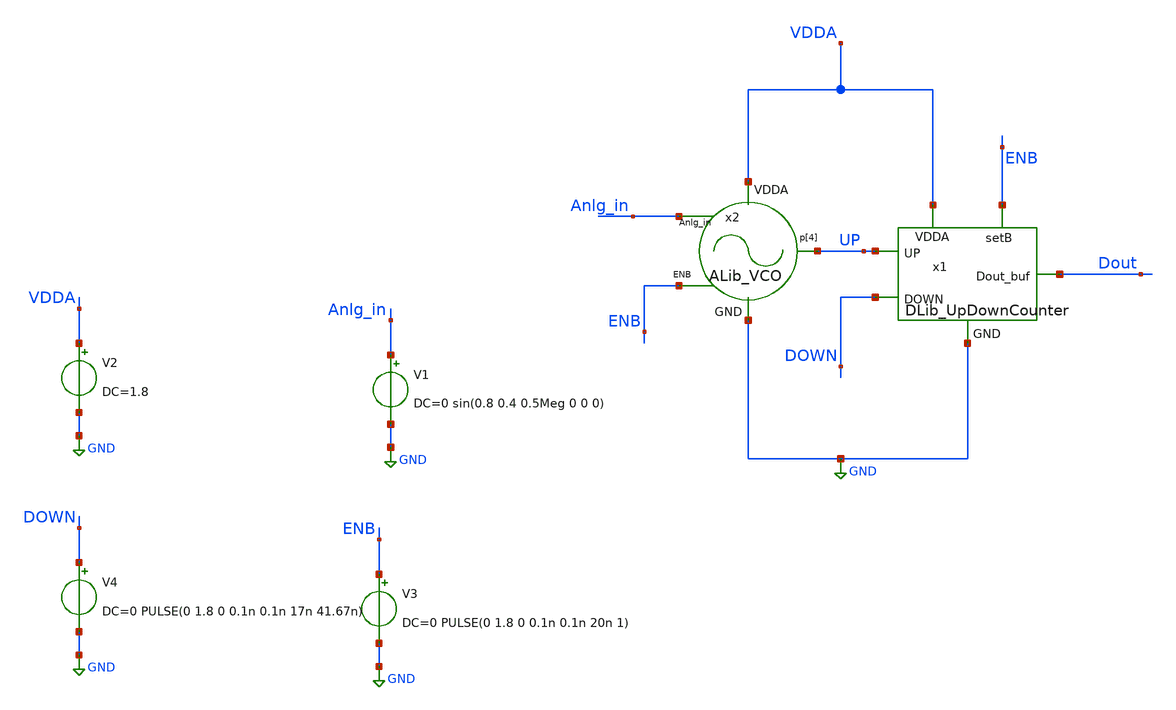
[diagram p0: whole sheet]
** sch_path: xschem/tb/DLib_UpDownCounter_tb.sch
**.subckt DLib_UpDownCounter_tb
x2 Anlg_in ENB UP VDDA GND ALib_VCO
x1 UP DOWN ENB Dout VDDA GND DLib_UpDownCounter
V1 Anlg_in GND DC=0 sin(0.8 0.4 0.5Meg 0 0 0)
V2 VDDA GND DC=1.8
V3 ENB GND DC=0 PULSE(0 1.8 0 0.1n 0.1n 20n 1)
V4 DOWN GND DC=0 PULSE(0 1.8 0 0.1n 0.1n 17n 41.67n)
**** begin user architecture code


.lib /home/dkits/openpdks/sky130A/libs.tech/ngspice/sky130.lib.spice tt
.inc /home/dkits/openpdks/sky130A/libs.ref/sky130_fd_sc_hd/spice/sky130_fd_sc_hd.spice




.control
set num_threads=10
save all
TRAN 1n 10u
.endc


**** end user architecture code
**.ends
.GLOBAL GND
.end
